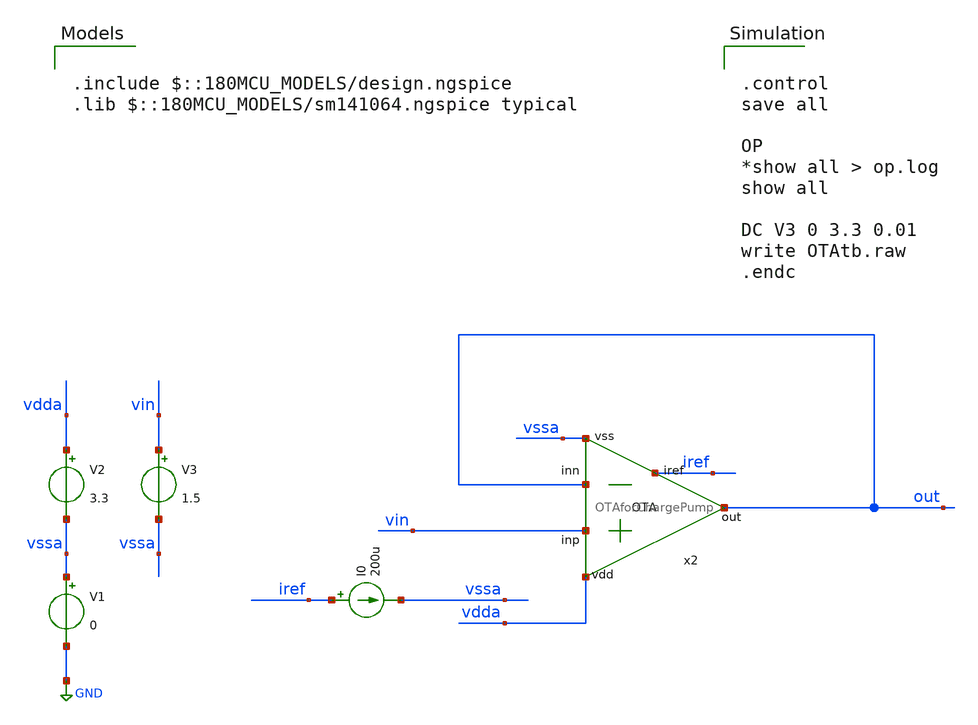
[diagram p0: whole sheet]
** sch_path: designs/libs/qw_core_analog_pkedit/OTAtb.sch
**.subckt OTAtb
V1 vssa GND 0
V2 vdda vssa 3.3
I0 iref vssa 200u
V3 vin vssa 1.5
x2 vdda iref vin out out vssa OTAforChargePump
**** begin user architecture code


.control
save all

OP
*show all > op.log
show all

DC V3 0 3.3 0.01
write OTAtb.raw
.endc



.include $::180MCU_MODELS/design.ngspice
.lib $::180MCU_MODELS/sm141064.ngspice typical

**** end user architecture code
**.ends

* expanding   symbol:  libs/qw_core_analog/OTAforChargePump/OTAforChargePump.sym # of pins=6
** sym_path: designs/libs/qw_core_analog_pkedit/OTAforChargePump/OTAforChargePump.sym
** sch_path: designs/libs/qw_core_analog_pkedit/OTAforChargePump/OTAforChargePump.sch
.subckt OTAforChargePump vdd iref inp inn out vss
*.iopin inp
*.iopin inn
*.iopin vdd
*.iopin vss
*.iopin out
*.iopin iref
XM8 iref iref vdd vdd pfet_03v3 L=0.28u W=40u nf=1 ad='int((nf+1)/2) * W/nf * 0.18u' as='int((nf+2)/2) * W/nf * 0.18u'
+ pd='2*int((nf+1)/2) * (W/nf + 0.18u)' ps='2*int((nf+2)/2) * (W/nf + 0.18u)' nrd='0.18u / W' nrs='0.18u / W'
+ sa=0 sb=0 sd=0 m=1
XM1 net1 iref vdd vdd pfet_03v3 L=0.28u W=40u nf=1 ad='int((nf+1)/2) * W/nf * 0.18u' as='int((nf+2)/2) * W/nf * 0.18u'
+ pd='2*int((nf+1)/2) * (W/nf + 0.18u)' ps='2*int((nf+2)/2) * (W/nf + 0.18u)' nrd='0.18u / W' nrs='0.18u / W'
+ sa=0 sb=0 sd=0 m=1
XM2 net2 inp net1 vdd pfet_03v3 L=0.28u W=20u nf=1 ad='int((nf+1)/2) * W/nf * 0.18u' as='int((nf+2)/2) * W/nf * 0.18u'
+ pd='2*int((nf+1)/2) * (W/nf + 0.18u)' ps='2*int((nf+2)/2) * (W/nf + 0.18u)' nrd='0.18u / W' nrs='0.18u / W'
+ sa=0 sb=0 sd=0 m=1
XM3 out inn net1 vdd pfet_03v3 L=0.28u W=20u nf=1 ad='int((nf+1)/2) * W/nf * 0.18u' as='int((nf+2)/2) * W/nf * 0.18u'
+ pd='2*int((nf+1)/2) * (W/nf + 0.18u)' ps='2*int((nf+2)/2) * (W/nf + 0.18u)' nrd='0.18u / W' nrs='0.18u / W'
+ sa=0 sb=0 sd=0 m=1
XM4 net2 net2 vss vss nfet_03v3 L=0.28u W=8u nf=1 ad='int((nf+1)/2) * W/nf * 0.18u' as='int((nf+2)/2) * W/nf * 0.18u'
+ pd='2*int((nf+1)/2) * (W/nf + 0.18u)' ps='2*int((nf+2)/2) * (W/nf + 0.18u)' nrd='0.18u / W' nrs='0.18u / W'
+ sa=0 sb=0 sd=0 m=1
XM5 out net2 vss vss nfet_03v3 L=0.28u W=8u nf=1 ad='int((nf+1)/2) * W/nf * 0.18u' as='int((nf+2)/2) * W/nf * 0.18u'
+ pd='2*int((nf+1)/2) * (W/nf + 0.18u)' ps='2*int((nf+2)/2) * (W/nf + 0.18u)' nrd='0.18u / W' nrs='0.18u / W'
+ sa=0 sb=0 sd=0 m=1
.ends

.GLOBAL GND
.end
